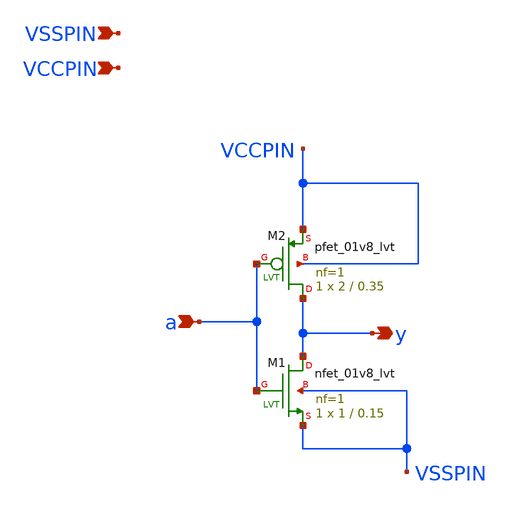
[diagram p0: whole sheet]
** sch_path: lvtNOT.sch
**.subckt lvtNOT a y VSSPIN VCCPIN
*.ipin a
*.opin y
*.ipin VSSPIN
*.ipin VCCPIN
XM2 y a VCCPIN VCCPIN sky130_fd_pr__pfet_01v8_lvt L=0.35 W=2 nf=1 ad='int((1 + 1)/2) * 2 / 1 * 0.29'
+ as='int((1 + 2)/2) * 2 / 1 * 0.29' pd='2*int((1 + 1)/2) * (2 / 1 + 0.29)' ps='2*int((1 + 2)/2) * (2 / 1 + 0.29)'
+ nrd='0.29 / 2 ' nrs='0.29 / 2 ' sa=0 sb=0 sd=0 mult=1 m=1
XM1 y a VSSPIN VSSPIN sky130_fd_pr__nfet_01v8_lvt L=0.15 W=1 nf=1 ad='int((nf+1)/2) * W/nf * 0.29' as='int((nf+2)/2) * W/nf * 0.29'
+ pd='2*int((nf+1)/2) * (W/nf + 0.29)' ps='2*int((nf+2)/2) * (W/nf + 0.29)' nrd='0.29 / W' nrs='0.29 / W'
+ sa=0 sb=0 sd=0 mult=1 m=1
**.ends
.end
